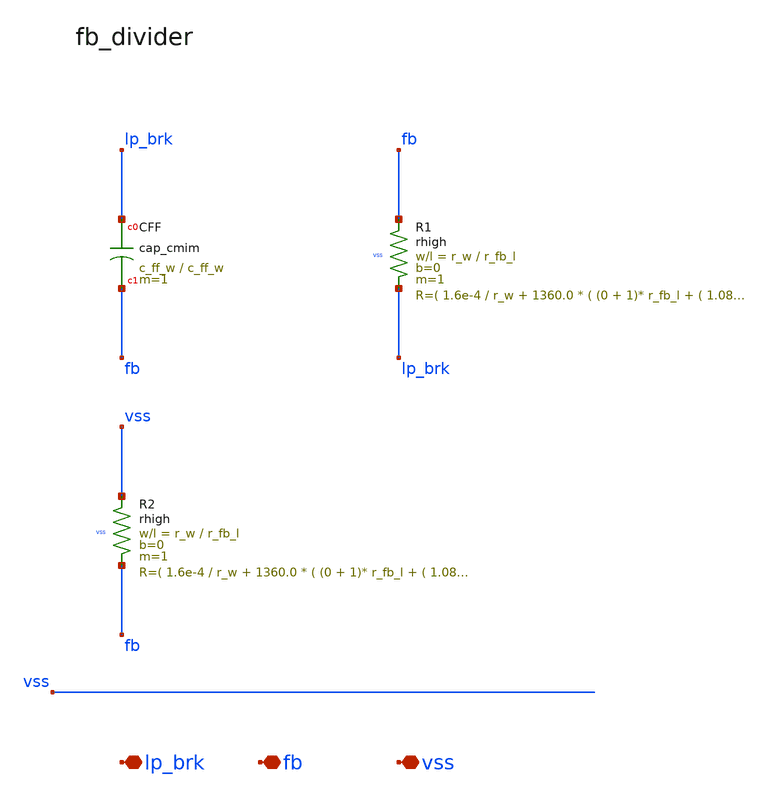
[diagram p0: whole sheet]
** sch_path: circuits/ldo_ihp_capless/xschem/blocks/fb_divider.sch
**.subckt fb_divider lp_brk fb vss
*.iopin lp_brk
*.iopin fb
*.iopin vss
XR1 fb lp_brk vss rhigh w=r_w l=r_fb_l m=1 b=0 mm_ok=1
XR2 vss fb vss rhigh w=r_w l=r_fb_l m=1 b=0 mm_ok=1
XCFF lp_brk fb cap_cmim w=c_ff_w l=c_ff_w m=1 mm_ok=1
**.ends
.end
